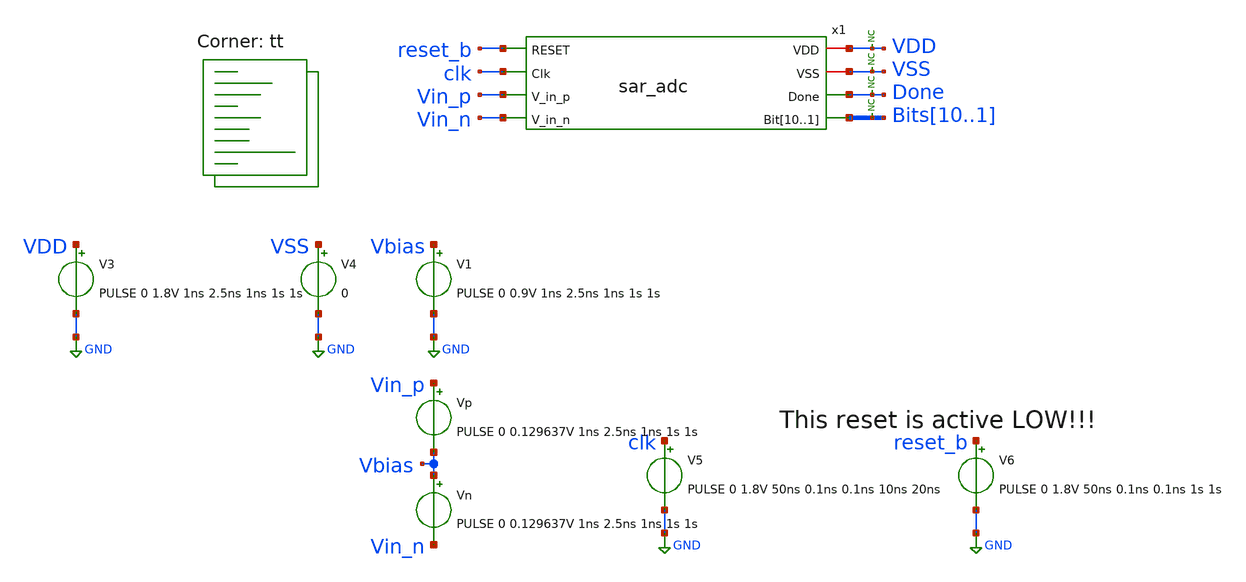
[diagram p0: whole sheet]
** sch_path: xschem/tests/sar_adc/sar_adc_max_sample_power_test.sch
**.subckt sar_adc_max_sample_power_test
V3 VDD GND PULSE 0 1.8V 1ns 2.5ns 1ns 1s 1s
V4 VSS GND 0
x1 VDD VSS reset_b clk Vin_p Vin_n Done Bits10 Bits9 Bits8 Bits7 Bits6 Bits5 Bits4 Bits3 Bits2 Bits1
+ sar_adc
Vn Vbias Vin_n PULSE 0 0.129637V 1ns 2.5ns 1ns 1s 1s
V5 clk GND PULSE 0 1.8V 50ns 0.1ns 0.1ns 10ns 20ns
V6 reset_b GND PULSE 0 1.8V 50ns 0.1ns 0.1ns 1s 1s
V1 Vbias GND PULSE 0 0.9V 1ns 2.5ns 1ns 1s 1s
Vp Vin_p Vbias PULSE 0 0.129637V 1ns 2.5ns 1ns 1s 1s
* noconn VDD
* noconn VSS
* noconn Done
* noconn Bits[10..1]
**** begin user architecture code

*.lib $::SKYWATER_MODELS/sky130.lib.spice tt

* .lib $::SKYWATER_MODELS/sky130.lib.spice.tt.red tt

.include $::SKYWATER_STDCELLS/sky130_fd_sc_hd.spice

.lib $::SKYWATER_MODELS/sky130.lib.spice tt



* ngspice commands
.options list acct opts
.control
save all
tran 0.5n 2.61us uic
let pow = -i(v3)*vdd

meas tran inst_pow MAX pow from=50n to=2.61u
meas tran avg_pow  AVG pow from=50n to=2.61u

plot -i(v3)*vdd
.endc



**** end user architecture code
**.ends
.GLOBAL GND
.end
